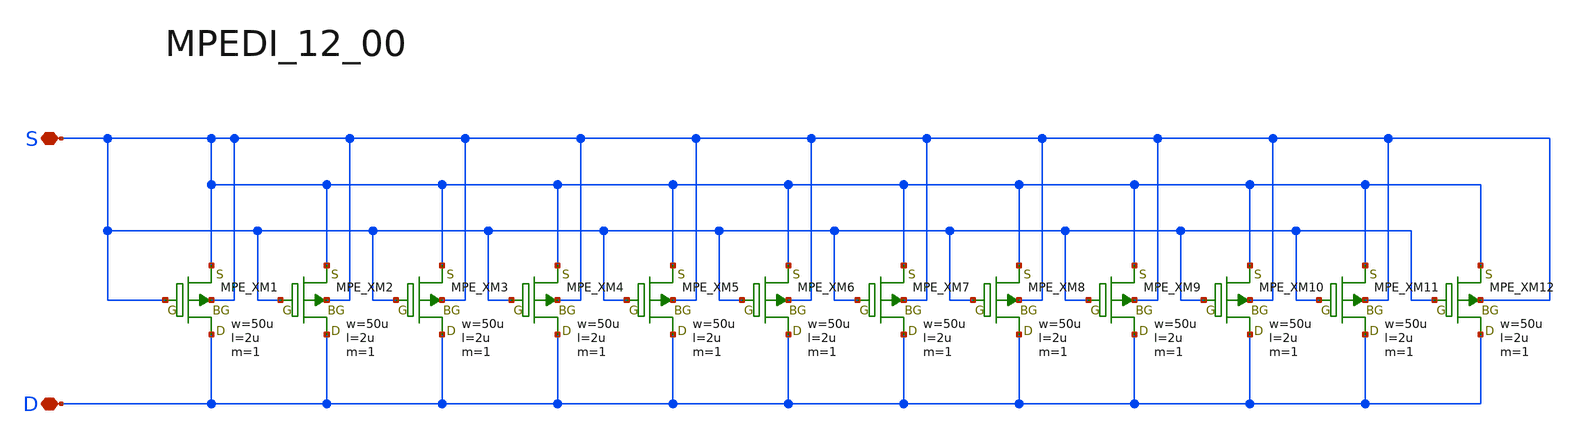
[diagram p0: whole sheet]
** sch_path: openIP62_rev1.0/IP62/Technology/tech/symbols/Xschem/IP62_2_ESD/MPEDI_12_00.sch
**.subckt MPEDI_12_00 S D
*.iopin S
*.iopin D
XM1 D S S S MPE w=50u l=2u as=0 ad=0 ps=0 pd=0 nrd=0 nrs=0 m=1
XM2 D S S S MPE w=50u l=2u as=0 ad=0 ps=0 pd=0 nrd=0 nrs=0 m=1
XM3 D S S S MPE w=50u l=2u as=0 ad=0 ps=0 pd=0 nrd=0 nrs=0 m=1
XM4 D S S S MPE w=50u l=2u as=0 ad=0 ps=0 pd=0 nrd=0 nrs=0 m=1
XM5 D S S S MPE w=50u l=2u as=0 ad=0 ps=0 pd=0 nrd=0 nrs=0 m=1
XM6 D S S S MPE w=50u l=2u as=0 ad=0 ps=0 pd=0 nrd=0 nrs=0 m=1
XM7 D S S S MPE w=50u l=2u as=0 ad=0 ps=0 pd=0 nrd=0 nrs=0 m=1
XM8 D S S S MPE w=50u l=2u as=0 ad=0 ps=0 pd=0 nrd=0 nrs=0 m=1
XM9 D S S S MPE w=50u l=2u as=0 ad=0 ps=0 pd=0 nrd=0 nrs=0 m=1
XM10 D S S S MPE w=50u l=2u as=0 ad=0 ps=0 pd=0 nrd=0 nrs=0 m=1
XM11 D S S S MPE w=50u l=2u as=0 ad=0 ps=0 pd=0 nrd=0 nrs=0 m=1
XM12 D S S S MPE w=50u l=2u as=0 ad=0 ps=0 pd=0 nrd=0 nrs=0 m=1
**.ends
.end
